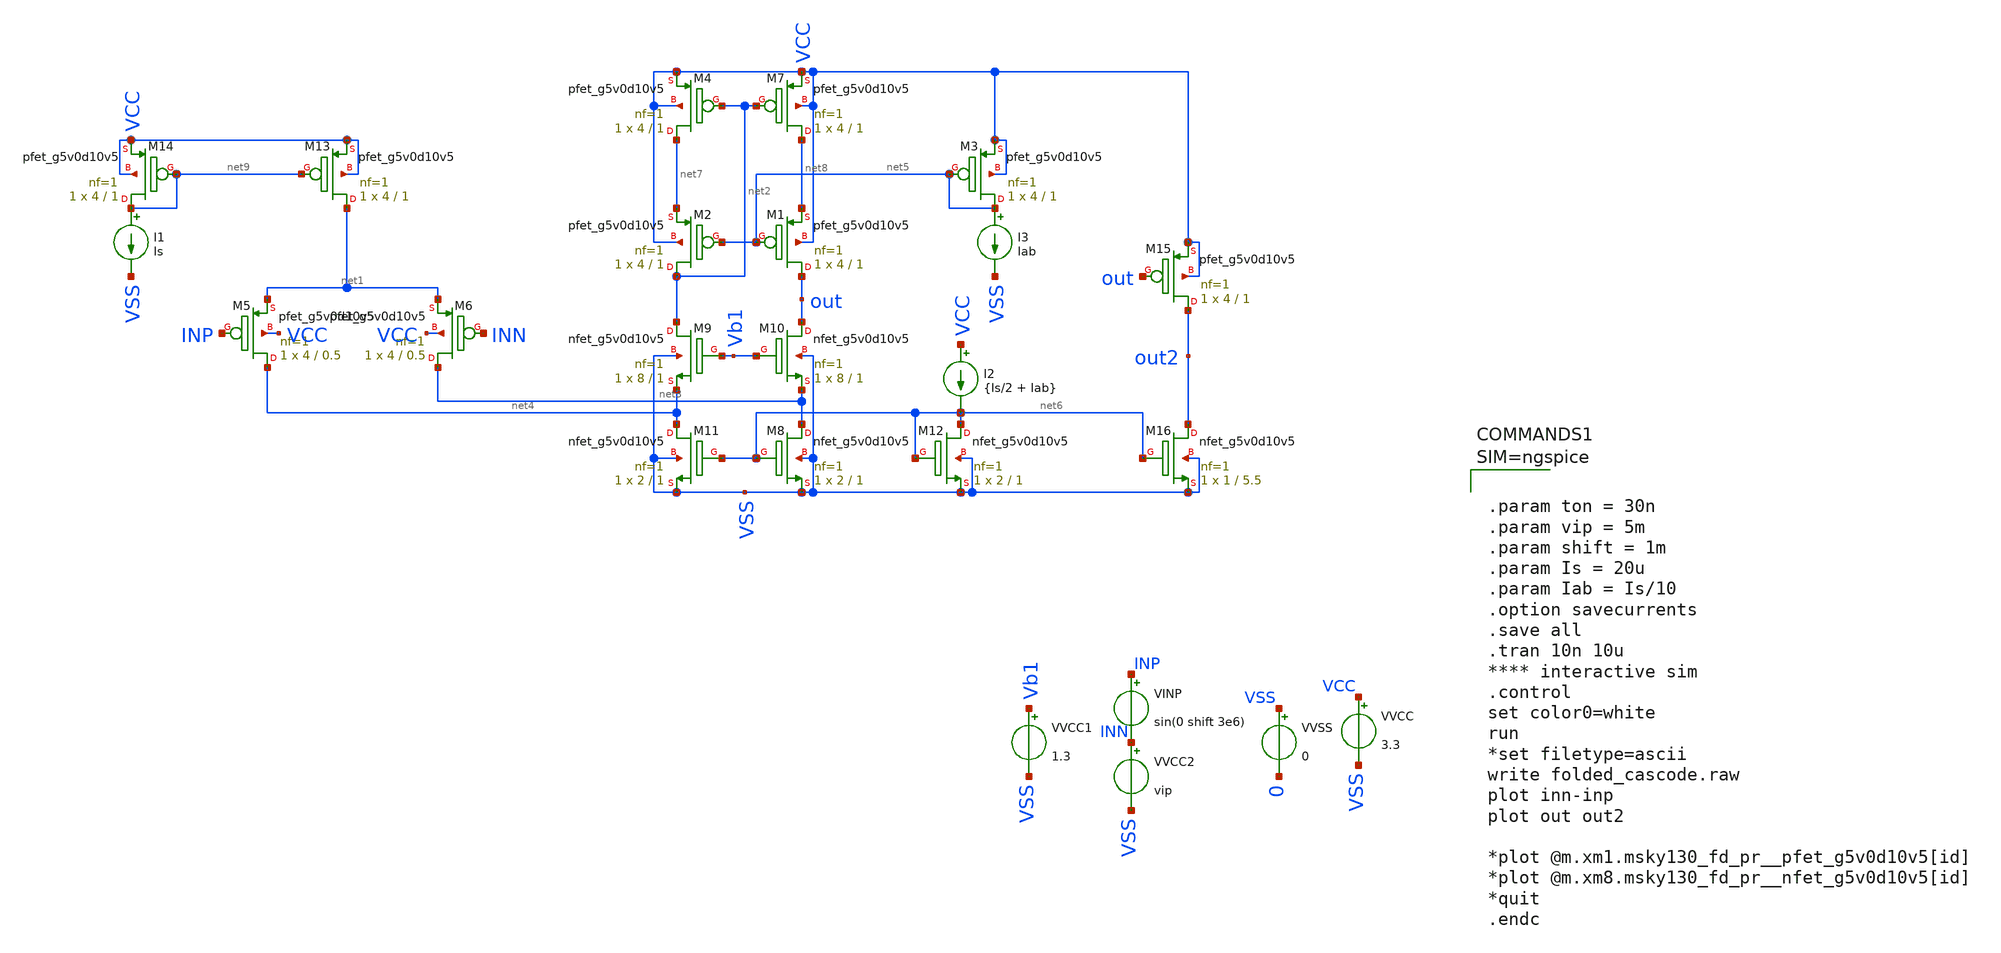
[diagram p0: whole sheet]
** sch_path: folded_cascode/folded_cascode.sch
.lib $::SKYWATER_MODELS/sky130.lib.spice.ss.red ss
.include $::SKYWATER_STDCELLS/sky130_fd_sc_hd.spice

**.subckt folded_cascode
VINP INP INN sin(0 shift 3e6)
VVSS VSS 0 0
VVCC VCC VSS 3.3
VVCC2 INN VSS vip
XM5 net4 INP net1 VCC sky130_fd_pr__pfet_g5v0d10v5 L=0.5 W=4 nf=1 ad='int((nf+1)/2) * W/nf * 0.29' as='int((nf+2)/2) * W/nf * 0.29'
+ pd='2*int((nf+1)/2) * (W/nf + 0.29)' ps='2*int((nf+2)/2) * (W/nf + 0.29)' nrd='0.29 / W' nrs='0.29 / W'
+ sa=0 sb=0 sd=0 mult=1 m=1
XM6 net3 INN net1 VCC sky130_fd_pr__pfet_g5v0d10v5 L=0.5 W=4 nf=1 ad='int((nf+1)/2) * W/nf * 0.29' as='int((nf+2)/2) * W/nf * 0.29'
+ pd='2*int((nf+1)/2) * (W/nf + 0.29)' ps='2*int((nf+2)/2) * (W/nf + 0.29)' nrd='0.29 / W' nrs='0.29 / W'
+ sa=0 sb=0 sd=0 mult=1 m=1
XM9 net2 Vb1 net4 VSS sky130_fd_pr__nfet_g5v0d10v5 L=1 W=8 nf=1 ad='int((nf+1)/2) * W/nf * 0.29' as='int((nf+2)/2) * W/nf * 0.29'
+ pd='2*int((nf+1)/2) * (W/nf + 0.29)' ps='2*int((nf+2)/2) * (W/nf + 0.29)' nrd='0.29 / W' nrs='0.29 / W'
+ sa=0 sb=0 sd=0 mult=1 m=1
XM10 out Vb1 net3 VSS sky130_fd_pr__nfet_g5v0d10v5 L=1 W=8 nf=1 ad='int((nf+1)/2) * W/nf * 0.29' as='int((nf+2)/2) * W/nf * 0.29'
+ pd='2*int((nf+1)/2) * (W/nf + 0.29)' ps='2*int((nf+2)/2) * (W/nf + 0.29)' nrd='0.29 / W' nrs='0.29 / W'
+ sa=0 sb=0 sd=0 mult=1 m=1
VVCC1 Vb1 VSS 1.3
I3 net5 VSS Iab
I2 VCC net6 {Is/2 + Iab}
XM3 net5 net5 VCC VCC sky130_fd_pr__pfet_g5v0d10v5 L=1 W=4 nf=1 ad='int((nf+1)/2) * W/nf * 0.29' as='int((nf+2)/2) * W/nf * 0.29'
+ pd='2*int((nf+1)/2) * (W/nf + 0.29)' ps='2*int((nf+2)/2) * (W/nf + 0.29)' nrd='0.29 / W' nrs='0.29 / W'
+ sa=0 sb=0 sd=0 mult=1 m=1
XM8 net3 net6 VSS VSS sky130_fd_pr__nfet_g5v0d10v5 L=1 W=2 nf=1 ad='int((nf+1)/2) * W/nf * 0.29' as='int((nf+2)/2) * W/nf * 0.29'
+ pd='2*int((nf+1)/2) * (W/nf + 0.29)' ps='2*int((nf+2)/2) * (W/nf + 0.29)' nrd='0.29 / W' nrs='0.29 / W'
+ sa=0 sb=0 sd=0 mult=1 m=1
XM11 net4 net6 VSS VSS sky130_fd_pr__nfet_g5v0d10v5 L=1 W=2 nf=1 ad='int((nf+1)/2) * W/nf * 0.29' as='int((nf+2)/2) * W/nf * 0.29'
+ pd='2*int((nf+1)/2) * (W/nf + 0.29)' ps='2*int((nf+2)/2) * (W/nf + 0.29)' nrd='0.29 / W' nrs='0.29 / W'
+ sa=0 sb=0 sd=0 mult=1 m=1
XM12 net6 net6 VSS VSS sky130_fd_pr__nfet_g5v0d10v5 L=1 W=2 nf=1 ad='int((nf+1)/2) * W/nf * 0.29' as='int((nf+2)/2) * W/nf * 0.29'
+ pd='2*int((nf+1)/2) * (W/nf + 0.29)' ps='2*int((nf+2)/2) * (W/nf + 0.29)' nrd='0.29 / W' nrs='0.29 / W'
+ sa=0 sb=0 sd=0 mult=1 m=1
XM1 out net5 net8 VCC sky130_fd_pr__pfet_g5v0d10v5 L=1 W=4 nf=1 ad='int((nf+1)/2) * W/nf * 0.29' as='int((nf+2)/2) * W/nf * 0.29'
+ pd='2*int((nf+1)/2) * (W/nf + 0.29)' ps='2*int((nf+2)/2) * (W/nf + 0.29)' nrd='0.29 / W' nrs='0.29 / W'
+ sa=0 sb=0 sd=0 mult=1 m=1
XM2 net2 net5 net7 VCC sky130_fd_pr__pfet_g5v0d10v5 L=1 W=4 nf=1 ad='int((nf+1)/2) * W/nf * 0.29' as='int((nf+2)/2) * W/nf * 0.29'
+ pd='2*int((nf+1)/2) * (W/nf + 0.29)' ps='2*int((nf+2)/2) * (W/nf + 0.29)' nrd='0.29 / W' nrs='0.29 / W'
+ sa=0 sb=0 sd=0 mult=1 m=1
XM4 net7 net2 VCC VCC sky130_fd_pr__pfet_g5v0d10v5 L=1 W=4 nf=1 ad='int((nf+1)/2) * W/nf * 0.29' as='int((nf+2)/2) * W/nf * 0.29'
+ pd='2*int((nf+1)/2) * (W/nf + 0.29)' ps='2*int((nf+2)/2) * (W/nf + 0.29)' nrd='0.29 / W' nrs='0.29 / W'
+ sa=0 sb=0 sd=0 mult=1 m=1
XM7 net8 net2 VCC VCC sky130_fd_pr__pfet_g5v0d10v5 L=1 W=4 nf=1 ad='int((nf+1)/2) * W/nf * 0.29' as='int((nf+2)/2) * W/nf * 0.29'
+ pd='2*int((nf+1)/2) * (W/nf + 0.29)' ps='2*int((nf+2)/2) * (W/nf + 0.29)' nrd='0.29 / W' nrs='0.29 / W'
+ sa=0 sb=0 sd=0 mult=1 m=1
XM13 net1 net9 VCC VCC sky130_fd_pr__pfet_g5v0d10v5 L=1 W=4 nf=1 ad='int((nf+1)/2) * W/nf * 0.29' as='int((nf+2)/2) * W/nf * 0.29'
+ pd='2*int((nf+1)/2) * (W/nf + 0.29)' ps='2*int((nf+2)/2) * (W/nf + 0.29)' nrd='0.29 / W' nrs='0.29 / W'
+ sa=0 sb=0 sd=0 mult=1 m=1
XM14 net9 net9 VCC VCC sky130_fd_pr__pfet_g5v0d10v5 L=1 W=4 nf=1 ad='int((nf+1)/2) * W/nf * 0.29' as='int((nf+2)/2) * W/nf * 0.29'
+ pd='2*int((nf+1)/2) * (W/nf + 0.29)' ps='2*int((nf+2)/2) * (W/nf + 0.29)' nrd='0.29 / W' nrs='0.29 / W'
+ sa=0 sb=0 sd=0 mult=1 m=1
I1 net9 VSS Is
XM15 out2 out VCC VCC sky130_fd_pr__pfet_g5v0d10v5 L=1 W=4 nf=1 ad='int((nf+1)/2) * W/nf * 0.29' as='int((nf+2)/2) * W/nf * 0.29'
+ pd='2*int((nf+1)/2) * (W/nf + 0.29)' ps='2*int((nf+2)/2) * (W/nf + 0.29)' nrd='0.29 / W' nrs='0.29 / W'
+ sa=0 sb=0 sd=0 mult=1 m=1
XM16 out2 net6 VSS VSS sky130_fd_pr__nfet_g5v0d10v5 L=5.5 W=1 nf=1 ad='int((nf+1)/2) * W/nf * 0.29' as='int((nf+2)/2) * W/nf * 0.29'
+ pd='2*int((nf+1)/2) * (W/nf + 0.29)' ps='2*int((nf+2)/2) * (W/nf + 0.29)' nrd='0.29 / W' nrs='0.29 / W'
+ sa=0 sb=0 sd=0 mult=1 m=1
**** begin user architecture code



.param ton = 30n
.param vip = 5m
.param shift = 1m
.param Is = 20u
.param Iab = Is/10
.option savecurrents
.save all
.tran 10n 10u
**** interactive sim
.control
set color0=white
run
*set filetype=ascii
write folded_cascode.raw
plot inn-inp
plot out out2

*plot @m.xm1.msky130_fd_pr__pfet_g5v0d10v5[id]
*plot @m.xm8.msky130_fd_pr__nfet_g5v0d10v5[id]
*quit
.endc



**** end user architecture code
**.ends
.end
